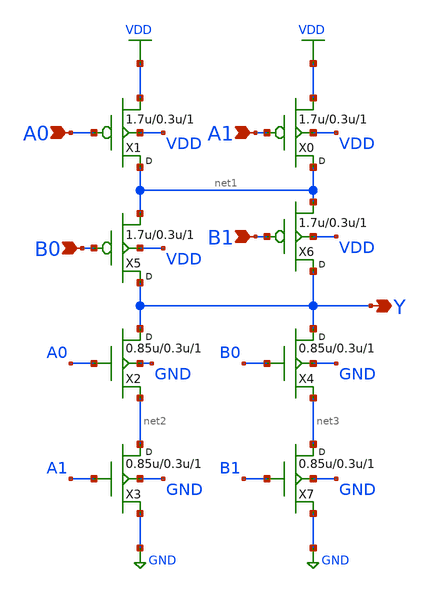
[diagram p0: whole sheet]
** sch_path: lib/12T/aoi221/gf180mcu_osu_sc_aoi22_1.sch
**.subckt gf180mcu_osu_sc_aoi22_1 A0 A1 B0 B1 Y
*.ipin A0
*.ipin A1
*.ipin B0
*.ipin B1
*.opin Y
X1 net1 A0 VDD VDD pmos_3p3 w=1.7u l=0.3u m=1
X0 net1 A1 VDD VDD pmos_3p3 w=1.7u l=0.3u m=1
X2 Y A0 net2 GND nmos_3p3 w=0.85u l=0.3u m=1
X3 net2 A1 GND GND nmos_3p3 w=0.85u l=0.3u m=1
X4 Y B0 net3 GND nmos_3p3 w=0.85u l=0.3u m=1
X5 Y B0 net1 VDD pmos_3p3 w=1.7u l=0.3u m=1
X6 Y B1 net1 VDD pmos_3p3 w=1.7u l=0.3u m=1
X7 net3 B1 GND GND nmos_3p3 w=0.85u l=0.3u m=1
**.ends
.GLOBAL VDD
.GLOBAL GND
.end
